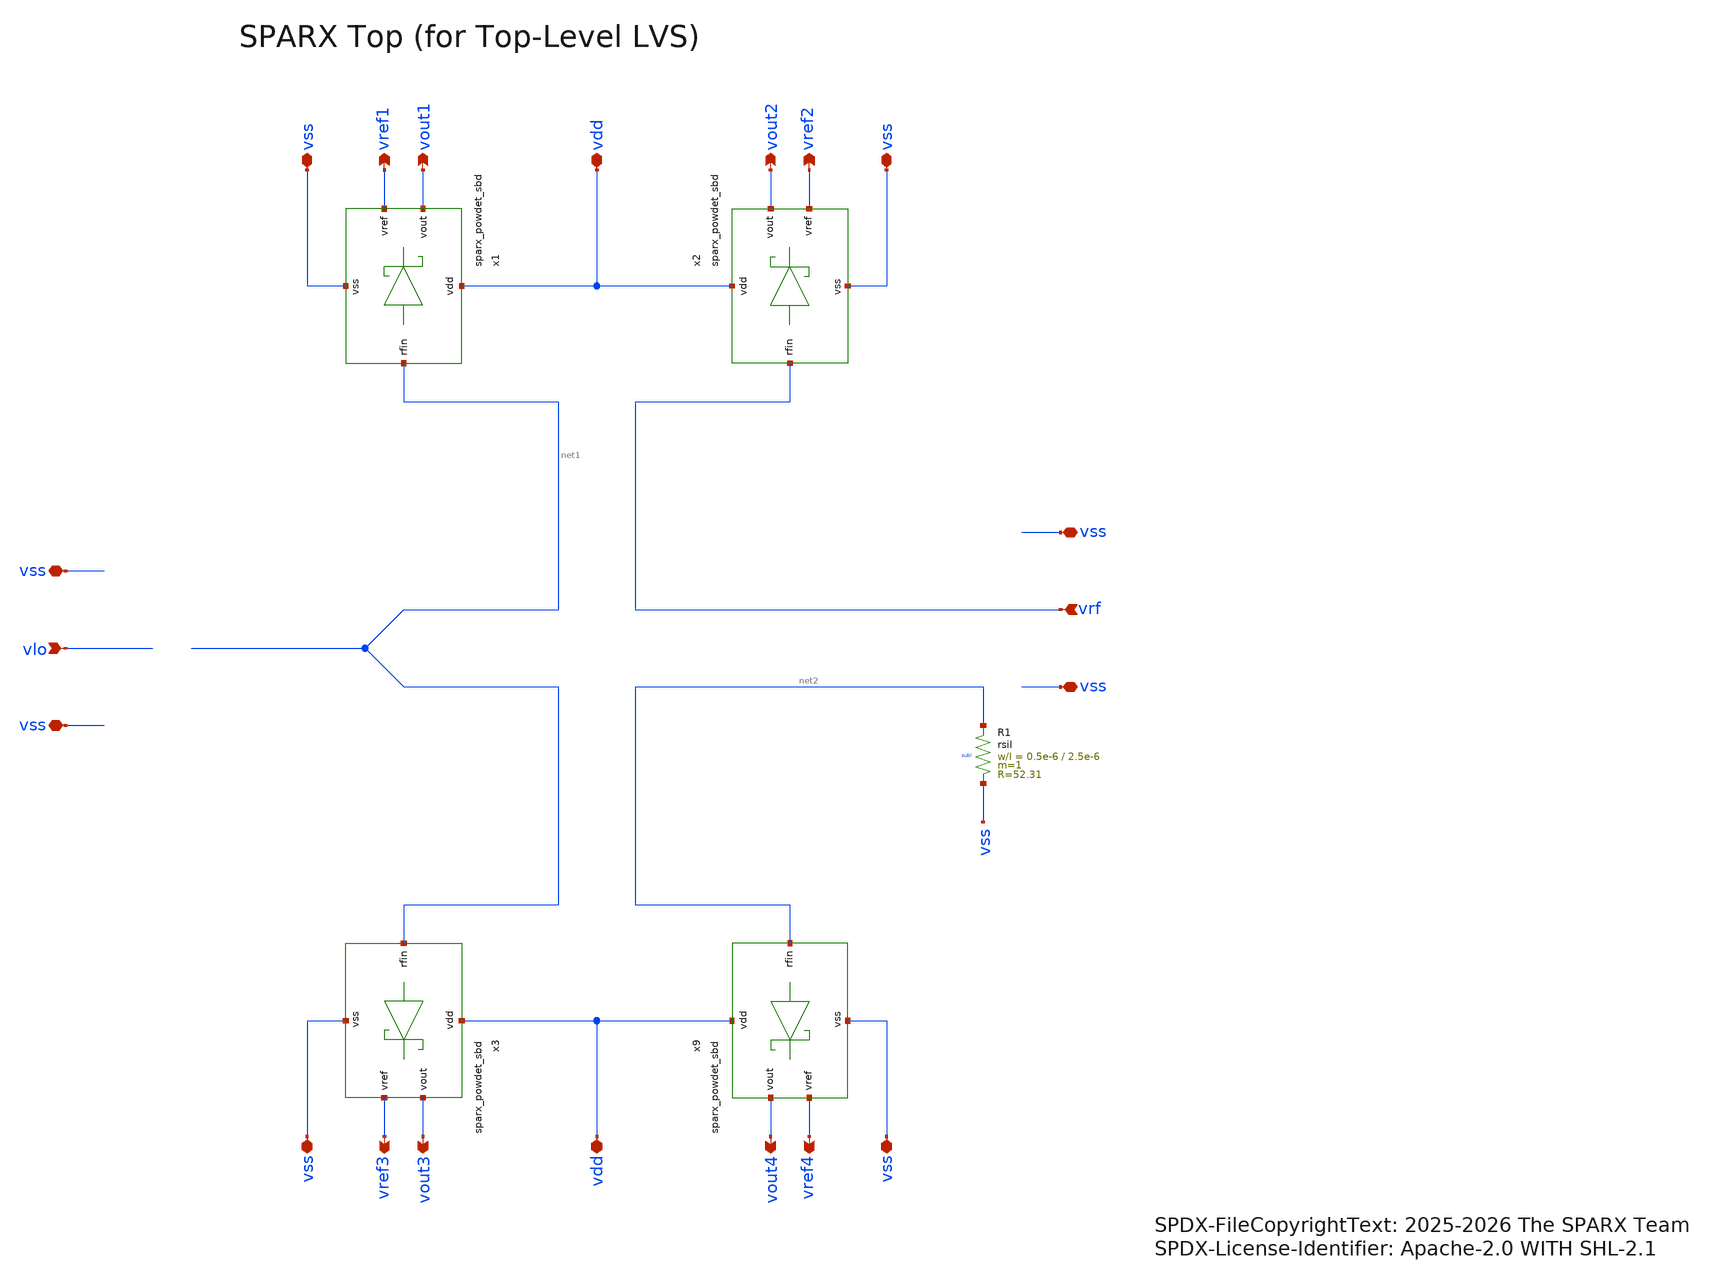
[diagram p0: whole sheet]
** sch_path: schematic/sparx_top_lvs.sch
* SPDX-FileCopyrightText: 2025-2026 The SPARX Team
* SPDX-License-Identifier: Apache-2.0 WITH SHL-2.1
**.subckt sparx_top_lvs vrf vout1 vdd vref1 vref2 vout2 vlo vss vss vout3 vdd vref3 vref4 vout4 vss
*+ vss vss vss vss vss
*.ipin vrf
*.opin vout1
*.iopin vdd
*.opin vref1
*.opin vref2
*.opin vout2
*.ipin vlo
*.iopin vss
*.iopin vss
*.opin vout3
*.iopin vdd
*.opin vref3
*.opin vref4
*.opin vout4
*.iopin vss
*.iopin vss
*.iopin vss
*.iopin vss
*.iopin vss
*.iopin vss
x1 vout1 vref1 vdd net1 vss sparx_powdet_sbd
x2 vout2 vref2 vdd vrf vss sparx_powdet_sbd
x3 vout3 vref3 vdd net1 vss sparx_powdet_sbd
x9 vout4 vref4 vdd net2 vss sparx_powdet_sbd
XR1 net2 vss sub! rsil w=0.5e-6 l=2.5e-6 m=1 mm_ok=1
**.ends
.end
